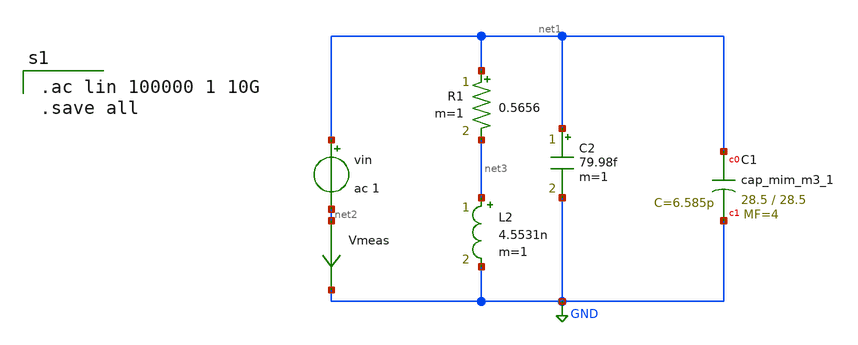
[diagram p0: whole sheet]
** sch_path: XSCHEM/ANTENNA/RLC_CSTXschem600.sch
**.subckt RLC_CSTXschem600
vin net1 net2 ac 1
XC1 net1 GND sky130_fd_pr__cap_mim_m3_1 W=28.5 L=28.5 MF=4 m=4
Vmeas net2 GND 0
.save i(vmeas)
R1 net1 net3 0.5656 m=1
L2 net3 GND 4.5531n m=1
C2 net1 GND 79.98f m=1
**** begin user architecture code

.ac lin 100000 1 10G
.save all


** opencircuitdesign pdks install
.lib $::SKYWATER_MODELS/sky130.lib.spice ff
.include /usr/local/share/pdk/sky130A/libs.ref/sky130_fd_sc_hd/spice/sky130_fd_sc_hd.spice

**** end user architecture code
**.ends
.GLOBAL GND
.end
